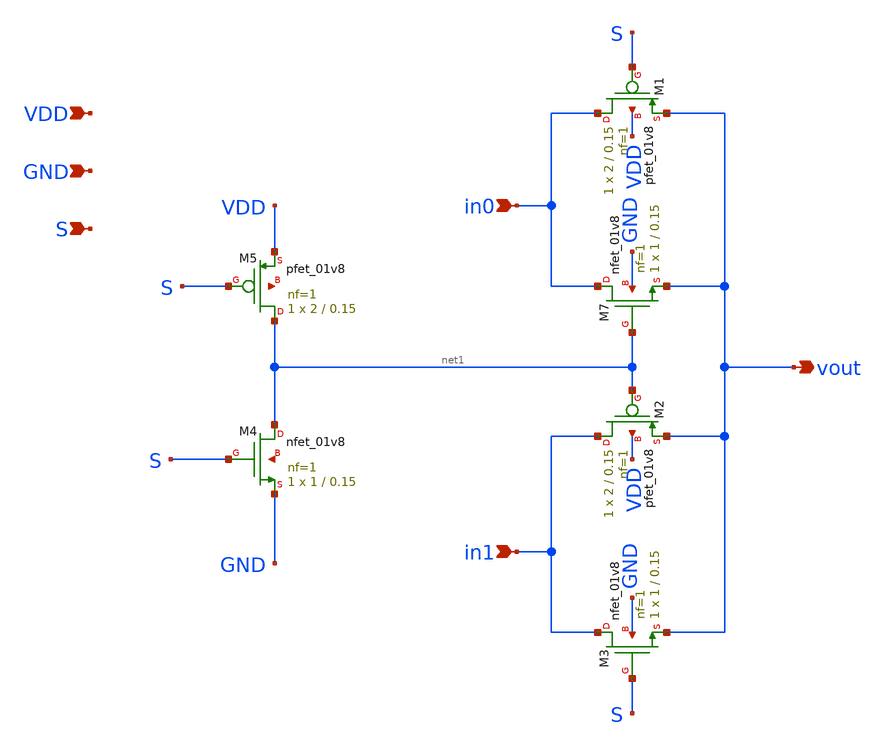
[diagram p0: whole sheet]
** sch_path: MUX/sky130_mux.sch
**.subckt sky130_mux VDD GND S in0 in1 vout
*.ipin VDD
*.ipin GND
*.ipin S
*.ipin in0
*.ipin in1
*.opin vout
XM1 in0 S vout VDD sky130_fd_pr__pfet_01v8 L=0.15 W=2 nf=1 ad='int((1 + 1)/2) * 2 / 1 * 0.29' as='int((1 + 2)/2) * 2 / 1 * 0.29'
+ pd='2*int((1 + 1)/2) * (2 / 1 + 0.29)' ps='2*int((1 + 2)/2) * (2 / 1 + 0.29)' nrd='0.29 / 2 ' nrs='0.29 / 2 '
+ sa=0 sb=0 sd=0 mult=1 m=1
XM2 in1 net1 vout VDD sky130_fd_pr__pfet_01v8 L=0.15 W=2 nf=1 ad='int((1 + 1)/2) * 2 / 1 * 0.29' as='int((1 + 2)/2) * 2 / 1 * 0.29'
+ pd='2*int((1 + 1)/2) * (2 / 1 + 0.29)' ps='2*int((1 + 2)/2) * (2 / 1 + 0.29)' nrd='0.29 / 2 ' nrs='0.29 / 2 '
+ sa=0 sb=0 sd=0 mult=1 m=1
XM5 net1 S VDD net2 sky130_fd_pr__pfet_01v8 L=0.15 W=2 nf=1 ad='int((1 + 1)/2) * 2 / 1 * 0.29' as='int((1 + 2)/2) * 2 / 1 * 0.29'
+ pd='2*int((1 + 1)/2) * (2 / 1 + 0.29)' ps='2*int((1 + 2)/2) * (2 / 1 + 0.29)' nrd='0.29 / 2 ' nrs='0.29 / 2 '
+ sa=0 sb=0 sd=0 mult=1 m=1
XM7 in0 net1 vout GND sky130_fd_pr__nfet_01v8 L=0.15 W=1 nf=1 ad='int((1 + 1)/2) * 1 / 1 * 0.29' as='int((1 + 2)/2) * 1 / 1 * 0.29'
+ pd='2*int((1 + 1)/2) * (1 / 1 + 0.29)' ps='2*int((1 + 2)/2) * (1 / 1 + 0.29)' nrd='0.29 / 1 ' nrs='0.29 / 1 '
+ sa=0 sb=0 sd=0 mult=1 m=1
XM3 in1 S vout GND sky130_fd_pr__nfet_01v8 L=0.15 W=1 nf=1 ad='int((1 + 1)/2) * 1 / 1 * 0.29' as='int((1 + 2)/2) * 1 / 1 * 0.29'
+ pd='2*int((1 + 1)/2) * (1 / 1 + 0.29)' ps='2*int((1 + 2)/2) * (1 / 1 + 0.29)' nrd='0.29 / 1 ' nrs='0.29 / 1 '
+ sa=0 sb=0 sd=0 mult=1 m=1
XM4 net1 S GND net3 sky130_fd_pr__nfet_01v8 L=0.15 W=1 nf=1 ad='int((1 + 1)/2) * 1 / 1 * 0.29' as='int((1 + 2)/2) * 1 / 1 * 0.29'
+ pd='2*int((1 + 1)/2) * (1 / 1 + 0.29)' ps='2*int((1 + 2)/2) * (1 / 1 + 0.29)' nrd='0.29 / 1 ' nrs='0.29 / 1 '
+ sa=0 sb=0 sd=0 mult=1 m=1
**.ends
.end
